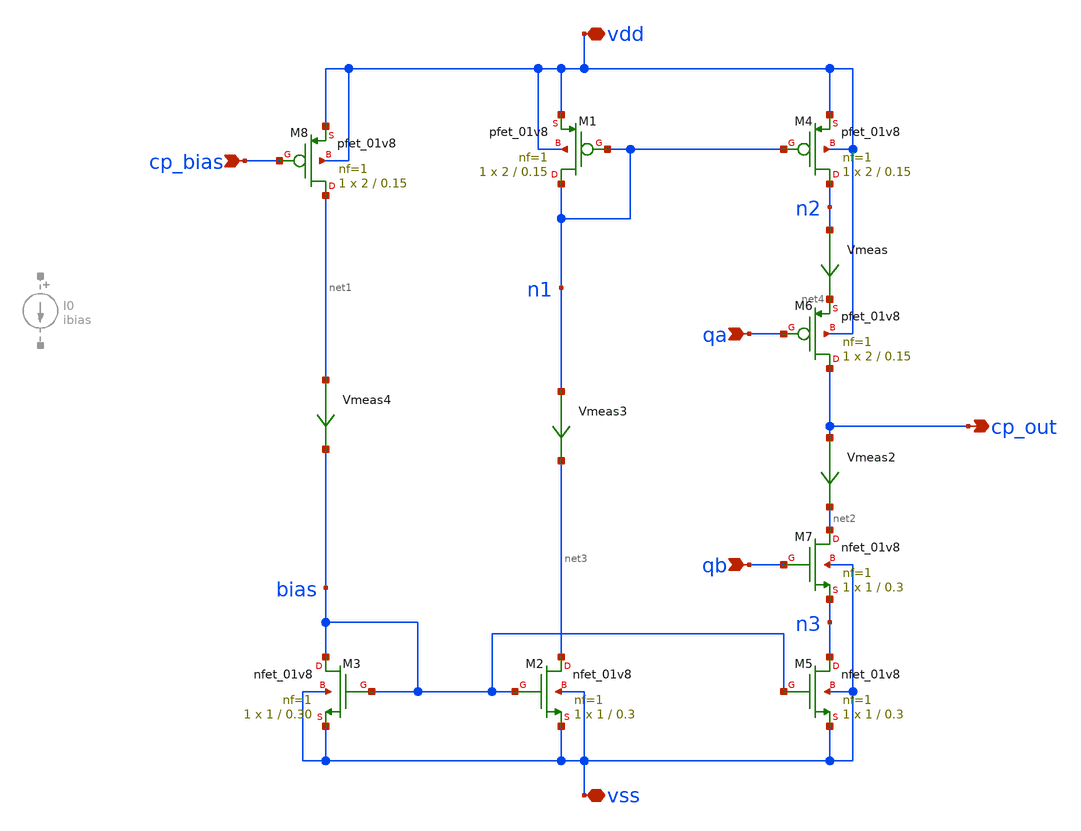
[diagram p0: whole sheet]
** sch_path: xschem/cp/cp.sch
**.subckt cp qa qb cp_out vdd vss cp_bias
*.ipin qa
*.ipin qb
*.opin cp_out
*.iopin vdd
*.iopin vss
*.ipin cp_bias
XM1 n1 n1 vdd vdd sky130_fd_pr__pfet_01v8 L=0.15 W=2 nf=1 ad='int((nf+1)/2) * W/nf * 0.29' as='int((nf+2)/2) * W/nf * 0.29'
+ pd='2*int((nf+1)/2) * (W/nf + 0.29)' ps='2*int((nf+2)/2) * (W/nf + 0.29)' nrd='0.29 / W' nrs='0.29 / W'
+ sa=0 sb=0 sd=0 mult=1 m=1
XM2 net3 bias vss vss sky130_fd_pr__nfet_01v8 L=0.3 W=1 nf=1 ad='int((nf+1)/2) * W/nf * 0.29' as='int((nf+2)/2) * W/nf * 0.29'
+ pd='2*int((nf+1)/2) * (W/nf + 0.29)' ps='2*int((nf+2)/2) * (W/nf + 0.29)' nrd='0.29 / W' nrs='0.29 / W'
+ sa=0 sb=0 sd=0 mult=1 m=1
XM3 bias bias vss vss sky130_fd_pr__nfet_01v8 L=0.30 W=1 nf=1 ad='int((nf+1)/2) * W/nf * 0.29' as='int((nf+2)/2) * W/nf * 0.29'
+ pd='2*int((nf+1)/2) * (W/nf + 0.29)' ps='2*int((nf+2)/2) * (W/nf + 0.29)' nrd='0.29 / W' nrs='0.29 / W'
+ sa=0 sb=0 sd=0 mult=1 m=1
XM4 n2 n1 vdd vdd sky130_fd_pr__pfet_01v8 L=0.15 W=2 nf=1 ad='int((nf+1)/2) * W/nf * 0.29' as='int((nf+2)/2) * W/nf * 0.29'
+ pd='2*int((nf+1)/2) * (W/nf + 0.29)' ps='2*int((nf+2)/2) * (W/nf + 0.29)' nrd='0.29 / W' nrs='0.29 / W'
+ sa=0 sb=0 sd=0 mult=1 m=1
XM5 n3 bias vss vss sky130_fd_pr__nfet_01v8 L=0.3 W=1 nf=1 ad='int((nf+1)/2) * W/nf * 0.29' as='int((nf+2)/2) * W/nf * 0.29'
+ pd='2*int((nf+1)/2) * (W/nf + 0.29)' ps='2*int((nf+2)/2) * (W/nf + 0.29)' nrd='0.29 / W' nrs='0.29 / W'
+ sa=0 sb=0 sd=0 mult=1 m=1
XM6 cp_out qa net4 vdd sky130_fd_pr__pfet_01v8 L=0.15 W=2 nf=1 ad='int((nf+1)/2) * W/nf * 0.29' as='int((nf+2)/2) * W/nf * 0.29'
+ pd='2*int((nf+1)/2) * (W/nf + 0.29)' ps='2*int((nf+2)/2) * (W/nf + 0.29)' nrd='0.29 / W' nrs='0.29 / W'
+ sa=0 sb=0 sd=0 mult=1 m=1
XM7 net2 qb n3 vss sky130_fd_pr__nfet_01v8 L=0.3 W=1 nf=1 ad='int((nf+1)/2) * W/nf * 0.29' as='int((nf+2)/2) * W/nf * 0.29'
+ pd='2*int((nf+1)/2) * (W/nf + 0.29)' ps='2*int((nf+2)/2) * (W/nf + 0.29)' nrd='0.29 / W' nrs='0.29 / W'
+ sa=0 sb=0 sd=0 mult=1 m=1
XM8 net1 cp_bias vdd vdd sky130_fd_pr__pfet_01v8 L=0.15 W=2 nf=1 ad='int((nf+1)/2) * W/nf * 0.29' as='int((nf+2)/2) * W/nf * 0.29'
+ pd='2*int((nf+1)/2) * (W/nf + 0.29)' ps='2*int((nf+2)/2) * (W/nf + 0.29)' nrd='0.29 / W' nrs='0.29 / W'
+ sa=0 sb=0 sd=0 mult=1 m=1
Vmeas n2 net4 0
.save i(vmeas)
Vmeas2 cp_out net2 0
.save i(vmeas2)
Vmeas3 n1 net3 0
.save i(vmeas3)
Vmeas4 net1 bias 0
.save i(vmeas4)
**.ends
.end
